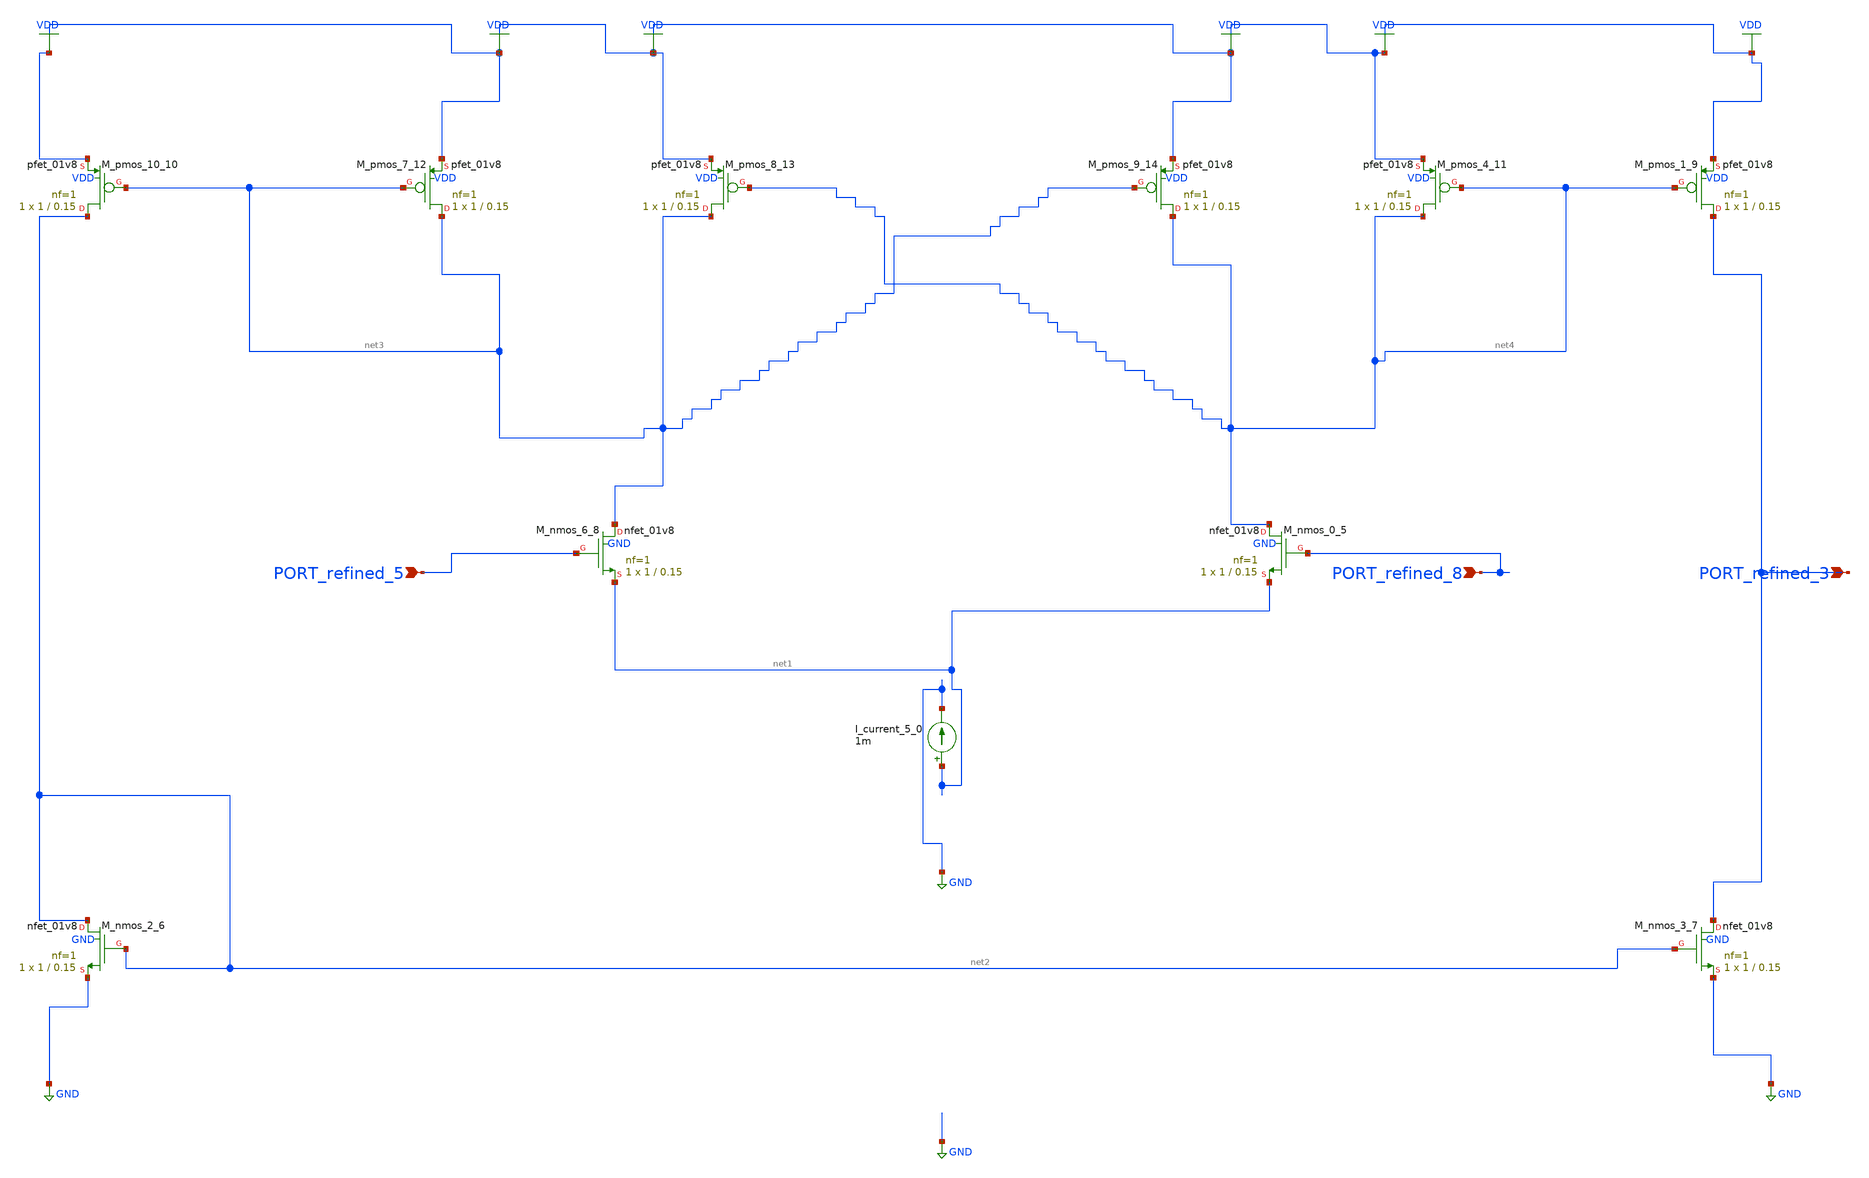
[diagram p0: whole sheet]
** sch_path: schematics/Image2Net/030.sch
**.subckt 030 PORT_refined_3 PORT_refined_5 PORT_refined_8
*.ipin PORT_refined_3
*.ipin PORT_refined_5
*.ipin PORT_refined_8
I_current_5_0 net1 GND 1m
XM_nmos_0_5 net4 PORT_refined_8 net1 GND sky130_fd_pr__nfet_01v8 L=0.15 W=1 nf=1 ad='int((1 + 1)/2) * 1 / 1 * 0.29'
+ as='int((1 + 2)/2) * 1 / 1 * 0.29' pd='2*int((1 + 1)/2) * (1 / 1 + 0.29)' ps='2*int((1 + 2)/2) * (1 / 1 + 0.29)'
+ nrd='0.29 / 1 ' nrs='0.29 / 1 ' sa=0 sb=0 sd=0 mult=1 m=1
XM_nmos_2_6 net2 net2 GND GND sky130_fd_pr__nfet_01v8 L=0.15 W=1 nf=1 ad='int((1 + 1)/2) * 1 / 1 * 0.29'
+ as='int((1 + 2)/2) * 1 / 1 * 0.29' pd='2*int((1 + 1)/2) * (1 / 1 + 0.29)' ps='2*int((1 + 2)/2) * (1 / 1 + 0.29)'
+ nrd='0.29 / 1 ' nrs='0.29 / 1 ' sa=0 sb=0 sd=0 mult=1 m=1
XM_nmos_3_7 PORT_refined_3 net2 GND GND sky130_fd_pr__nfet_01v8 L=0.15 W=1 nf=1 ad='int((1 + 1)/2) * 1 / 1 * 0.29'
+ as='int((1 + 2)/2) * 1 / 1 * 0.29' pd='2*int((1 + 1)/2) * (1 / 1 + 0.29)' ps='2*int((1 + 2)/2) * (1 / 1 + 0.29)'
+ nrd='0.29 / 1 ' nrs='0.29 / 1 ' sa=0 sb=0 sd=0 mult=1 m=1
XM_nmos_6_8 net3 PORT_refined_5 net1 GND sky130_fd_pr__nfet_01v8 L=0.15 W=1 nf=1 ad='int((1 + 1)/2) * 1 / 1 * 0.29'
+ as='int((1 + 2)/2) * 1 / 1 * 0.29' pd='2*int((1 + 1)/2) * (1 / 1 + 0.29)' ps='2*int((1 + 2)/2) * (1 / 1 + 0.29)'
+ nrd='0.29 / 1 ' nrs='0.29 / 1 ' sa=0 sb=0 sd=0 mult=1 m=1
XM_pmos_1_9 PORT_refined_3 net4 VDD VDD sky130_fd_pr__pfet_01v8 L=0.15 W=1 nf=1 ad='int((1 + 1)/2) * 1 / 1 * 0.29'
+ as='int((1 + 2)/2) * 1 / 1 * 0.29' pd='2*int((1 + 1)/2) * (1 / 1 + 0.29)' ps='2*int((1 + 2)/2) * (1 / 1 + 0.29)'
+ nrd='0.29 / 1 ' nrs='0.29 / 1 ' sa=0 sb=0 sd=0 mult=1 m=1
XM_pmos_10_10 net2 net3 VDD VDD sky130_fd_pr__pfet_01v8 L=0.15 W=1 nf=1 ad='int((1 + 1)/2) * 1 / 1 * 0.29'
+ as='int((1 + 2)/2) * 1 / 1 * 0.29' pd='2*int((1 + 1)/2) * (1 / 1 + 0.29)' ps='2*int((1 + 2)/2) * (1 / 1 + 0.29)'
+ nrd='0.29 / 1 ' nrs='0.29 / 1 ' sa=0 sb=0 sd=0 mult=1 m=1
XM_pmos_4_11 net4 net4 VDD VDD sky130_fd_pr__pfet_01v8 L=0.15 W=1 nf=1 ad='int((1 + 1)/2) * 1 / 1 * 0.29'
+ as='int((1 + 2)/2) * 1 / 1 * 0.29' pd='2*int((1 + 1)/2) * (1 / 1 + 0.29)' ps='2*int((1 + 2)/2) * (1 / 1 + 0.29)'
+ nrd='0.29 / 1 ' nrs='0.29 / 1 ' sa=0 sb=0 sd=0 mult=1 m=1
XM_pmos_7_12 net3 net3 VDD VDD sky130_fd_pr__pfet_01v8 L=0.15 W=1 nf=1 ad='int((1 + 1)/2) * 1 / 1 * 0.29'
+ as='int((1 + 2)/2) * 1 / 1 * 0.29' pd='2*int((1 + 1)/2) * (1 / 1 + 0.29)' ps='2*int((1 + 2)/2) * (1 / 1 + 0.29)'
+ nrd='0.29 / 1 ' nrs='0.29 / 1 ' sa=0 sb=0 sd=0 mult=1 m=1
XM_pmos_8_13 net3 net4 VDD VDD sky130_fd_pr__pfet_01v8 L=0.15 W=1 nf=1 ad='int((1 + 1)/2) * 1 / 1 * 0.29'
+ as='int((1 + 2)/2) * 1 / 1 * 0.29' pd='2*int((1 + 1)/2) * (1 / 1 + 0.29)' ps='2*int((1 + 2)/2) * (1 / 1 + 0.29)'
+ nrd='0.29 / 1 ' nrs='0.29 / 1 ' sa=0 sb=0 sd=0 mult=1 m=1
XM_pmos_9_14 net4 net3 VDD VDD sky130_fd_pr__pfet_01v8 L=0.15 W=1 nf=1 ad='int((1 + 1)/2) * 1 / 1 * 0.29'
+ as='int((1 + 2)/2) * 1 / 1 * 0.29' pd='2*int((1 + 1)/2) * (1 / 1 + 0.29)' ps='2*int((1 + 2)/2) * (1 / 1 + 0.29)'
+ nrd='0.29 / 1 ' nrs='0.29 / 1 ' sa=0 sb=0 sd=0 mult=1 m=1
**.ends
.GLOBAL GND
.GLOBAL VDD
.end
